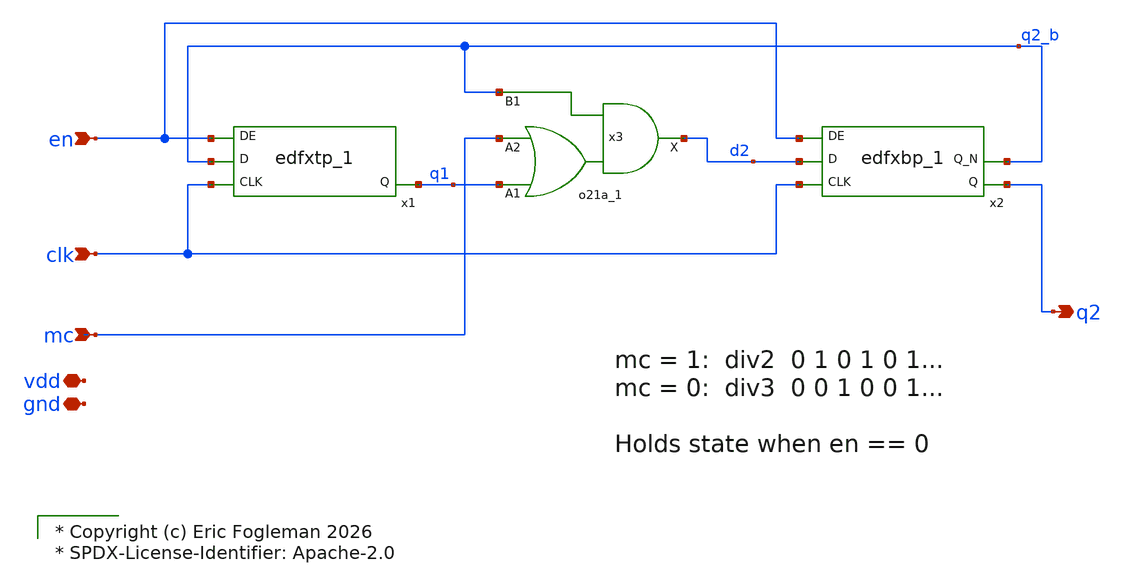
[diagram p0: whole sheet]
** sch_path: xschem/ejf_pll96_sdiv23.sch

* Copyright (c) Eric Fogleman 2026
* SPDX-License-Identifier: Apache-2.0

**.subckt ejf_pll96_sdiv23 clk mc q2 vdd gnd en
*.ipin clk
*.ipin mc
*.opin q2
*.iopin vdd
*.iopin gnd
*.ipin en
x3 q1 mc q2_b gnd gnd vdd vdd d2 sky130_fd_sc_ls__o21a_1
x1 clk q2_b en gnd gnd vdd vdd q1 sky130_fd_sc_ls__edfxtp_1
x2 clk d2 en gnd gnd vdd vdd q2 q2_b sky130_fd_sc_ls__edfxbp_1
**.ends
.end
